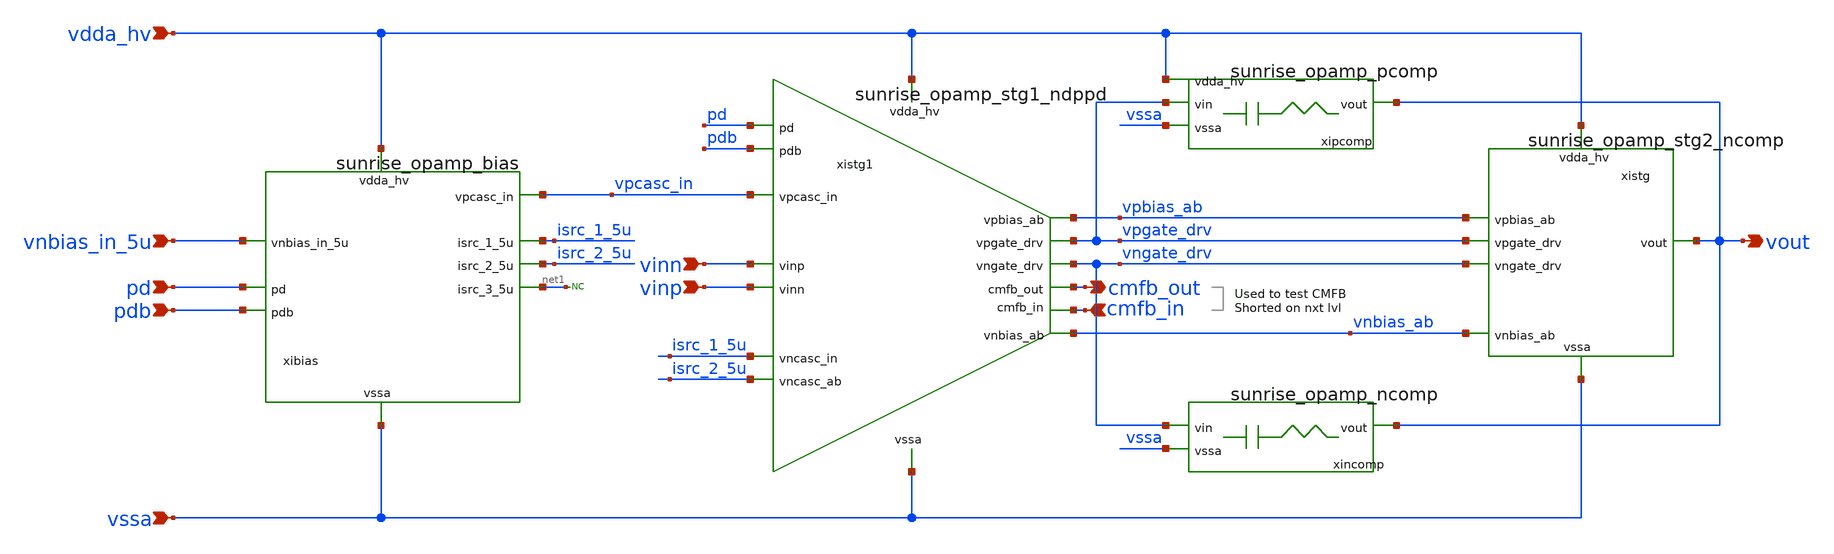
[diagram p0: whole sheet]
** sch_path: Schematics_Layout/sunrise_opamp_cmfb_prb_ndppd/sunrise_opamp_cmfb_prb_ndppd.sch
**.subckt sunrise_opamp_cmfb_prb_ndppd vinp vinn pd pdb vnbias_in_5u vssa vdda_hv vout cmfb_in
*+ cmfb_out
*.ipin vinp
*.ipin vinn
*.ipin pd
*.ipin pdb
*.ipin vnbias_in_5u
*.ipin vssa
*.ipin vdda_hv
*.opin vout
*.ipin cmfb_in
*.opin cmfb_out
xibias vdda_hv pdb vnbias_in_5u isrc_1_5u vpcasc_in pd vssa isrc_2_5u net1 sunrise_opamp_bias
xistg1 vdda_hv pdb vpcasc_in vpgate_drv vinp vinn pd vngate_drv cmfb_out cmfb_in isrc_1_5u vssa
+ vpbias_ab isrc_2_5u vnbias_ab sunrise_opamp_stg1_ndppd
* noconn #net1
xistg vdda_hv vpbias_ab vpgate_drv vout vngate_drv vnbias_ab vssa sunrise_opamp_stg2_ncomp
xincomp vssa vout vngate_drv sunrise_opamp_ncomp
xipcomp vssa vout vpgate_drv vdda_hv sunrise_opamp_pcomp
**.ends
.end
